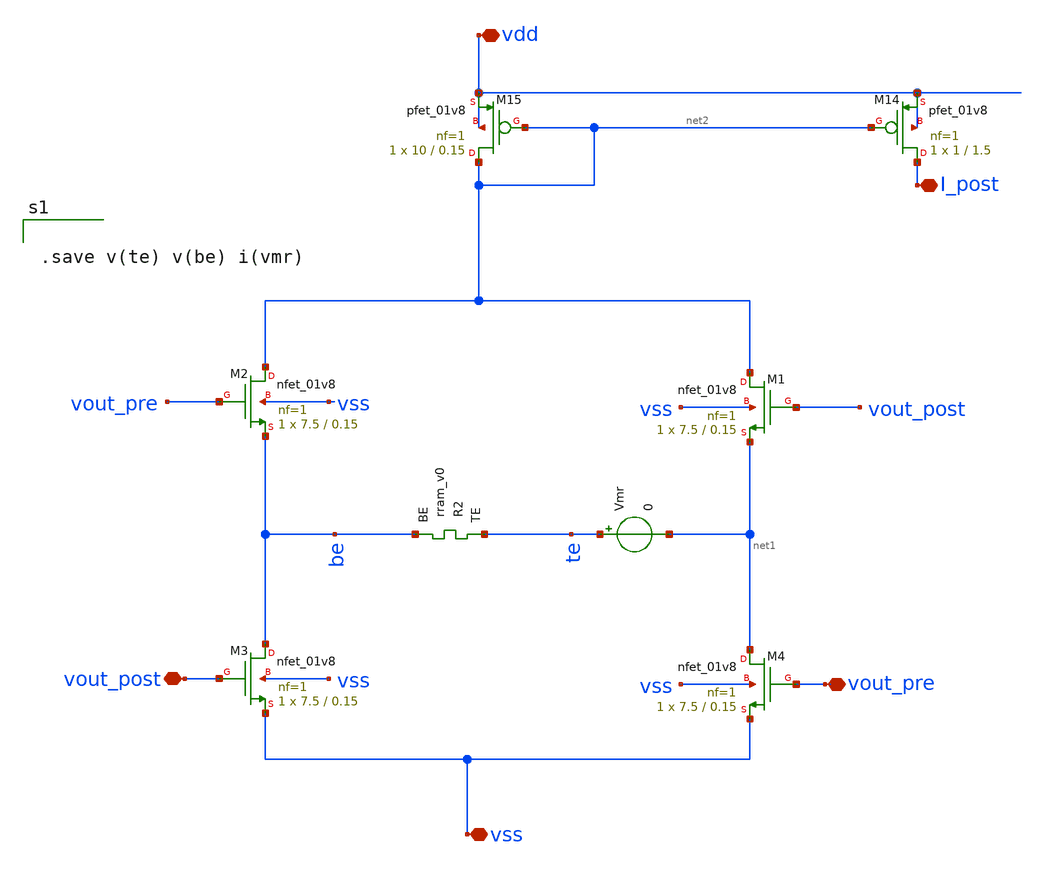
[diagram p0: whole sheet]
** sch_path: Synapse/stdp.sch
**.subckt stdp vdd vss vout_post vout_pre I_post
*.iopin vdd
*.iopin vss
*.iopin vout_post
*.iopin vout_pre
*.iopin I_post
XM2 net2 vout_pre be vss sky130_fd_pr__nfet_01v8 L=0.15 W=7.5 nf=1 ad='int((nf+1)/2) * W/nf * 0.29' as='int((nf+2)/2) * W/nf * 0.29'
+ pd='2*int((nf+1)/2) * (W/nf + 0.29)' ps='2*int((nf+2)/2) * (W/nf + 0.29)' nrd='0.29 / W' nrs='0.29 / W'
+ sa=0 sb=0 sd=0 mult=1 m=1
XM3 be vout_post vss vss sky130_fd_pr__nfet_01v8 L=0.15 W=7.5 nf=1 ad='int((nf+1)/2) * W/nf * 0.29' as='int((nf+2)/2) * W/nf * 0.29'
+ pd='2*int((nf+1)/2) * (W/nf + 0.29)' ps='2*int((nf+2)/2) * (W/nf + 0.29)' nrd='0.29 / W' nrs='0.29 / W'
+ sa=0 sb=0 sd=0 mult=1 m=1
XM4 net1 vout_pre vss vss sky130_fd_pr__nfet_01v8 L=0.15 W=7.5 nf=1 ad='int((nf+1)/2) * W/nf * 0.29'
+ as='int((nf+2)/2) * W/nf * 0.29' pd='2*int((nf+1)/2) * (W/nf + 0.29)' ps='2*int((nf+2)/2) * (W/nf + 0.29)'
+ nrd='0.29 / W' nrs='0.29 / W' sa=0 sb=0 sd=0 mult=1 m=1
XR2 te be rram_v0
XM14 I_post net2 vdd vdd sky130_fd_pr__pfet_01v8 L=1.5 W=1 nf=1 ad='int((nf+1)/2) * W/nf * 0.29' as='int((nf+2)/2) * W/nf * 0.29'
+ pd='2*int((nf+1)/2) * (W/nf + 0.29)' ps='2*int((nf+2)/2) * (W/nf + 0.29)' nrd='0.29 / W' nrs='0.29 / W'
+ sa=0 sb=0 sd=0 mult=1 m=1
XM15 net2 net2 vdd vdd sky130_fd_pr__pfet_01v8 L=0.15 W=10 nf=1 ad='int((nf+1)/2) * W/nf * 0.29' as='int((nf+2)/2) * W/nf * 0.29'
+ pd='2*int((nf+1)/2) * (W/nf + 0.29)' ps='2*int((nf+2)/2) * (W/nf + 0.29)' nrd='0.29 / W' nrs='0.29 / W'
+ sa=0 sb=0 sd=0 mult=1 m=1
Vmr te net1 0
.save i(vmr)
XM1 net2 vout_post net1 vss sky130_fd_pr__nfet_01v8 L=0.15 W=7.5 nf=1 ad='int((nf+1)/2) * W/nf * 0.29'
+ as='int((nf+2)/2) * W/nf * 0.29' pd='2*int((nf+1)/2) * (W/nf + 0.29)' ps='2*int((nf+2)/2) * (W/nf + 0.29)'
+ nrd='0.29 / W' nrs='0.29 / W' sa=0 sb=0 sd=0 mult=1 m=1
**** begin user architecture code


.save v(te) v(be) i(vmr)


**** end user architecture code
**.ends
.end
